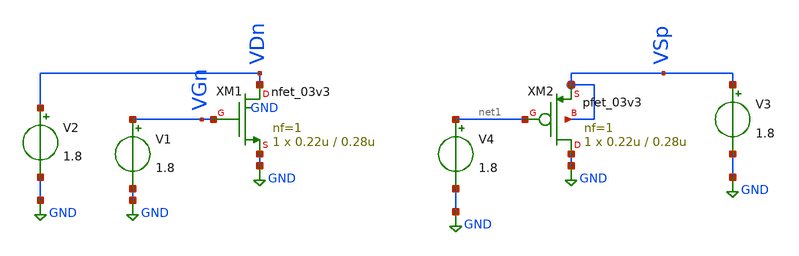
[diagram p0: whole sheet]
** sch_path: xschem/caracterizador/charac.sch
* Copyright 2022 GlobalFoundries PDK Authors
* Licensed under the Apache License, Version 2.0 (the "License");
* you may not use this file except in compliance with the License.
* You may obtain a copy of the License at
* https://www.apache.org/licenses/LICENSE-2.0
* Unless required by applicable law or agreed to in writing, software
* distributed under the License is distributed on an "AS IS" BASIS,
* WITHOUT WARRANTIES OR CONDITIONS OF ANY KIND, either express or implied.
* See the License for the specific language governing permissions and
* limitations under the License.
**.subckt charac
XM1 VDn VGn GND GND nfet_03v3 L=0.28u W=0.22u nf=1 ad='int((nf+1)/2) * W/nf * 0.18u' as='int((nf+2)/2) * W/nf * 0.18u'
+ pd='2*int((nf+1)/2) * (W/nf + 0.18u)' ps='2*int((nf+2)/2) * (W/nf + 0.18u)' nrd='0.18u / W' nrs='0.18u / W'
+ sa=0 sb=0 sd=0 m=1 par=1
XM2 GND net1 VSp VSp pfet_03v3 L=0.28u W=0.22u nf=1 ad='int((nf+1)/2) * W/nf * 0.18u' as='int((nf+2)/2) * W/nf * 0.18u'
+ pd='2*int((nf+1)/2) * (W/nf + 0.18u)' ps='2*int((nf+2)/2) * (W/nf + 0.18u)' nrd='0.18u / W' nrs='0.18u / W'
+ sa=0 sb=0 sd=0 m=1 par=1
V1 VGn GND 1.8
V2 VDn GND 1.8
V3 VSp GND 1.8
V4 net1 GND 1.8
**** begin user architecture code



.include /home/ringosinye/eda/pdks/gf180mcuD/libs.tech/ngspice/design.ngspice
.lib /home/ringosinye/eda/pdks/gf180mcuD/libs.tech/ngspice/sm141064.ngspice typical

.control
  save all

  * NMOS salida: Id vs Vds, varios Vgs
  dc V2 0 3.3 0.01 V1 0 3.3 0.55
  plot -i(V2) title 'NMOS Output' xlabel 'VDS (V)' ylabel 'ID (A)'



  * NMOS transferencia: Id vs Vgs, varios Vds
  dc V1 0 3.3 0.01 V2 0.55 3.3 0.55
  plot -i(V2) title 'NMOS Transfer' xlabel 'VGS (V)' ylabel 'ID (A)'



  * PMOS salida (V5 = 3.3 fija en la fuente): Vsd = 3.3 - V3
  dc V3 3.3 0 -0.01 V4 3.3 0 -0.55
  plot i(V3) title 'PMOS Output' xlabel 'V3 (V)  [VSD = 3.3 - V3]' ylabel 'ID (A)'



  * PMOS transferencia: Vsg = 3.3 - V4
  dc V4 3.3 0 -0.01 V3 2.75 0 -0.55
  plot i(V3) title 'PMOS Transfer' xlabel 'V4 (V)  [VSG = 3.3 - V4]' ylabel 'ID (A)'
.endc


**** end user architecture code
**.ends
.GLOBAL GND
.end
